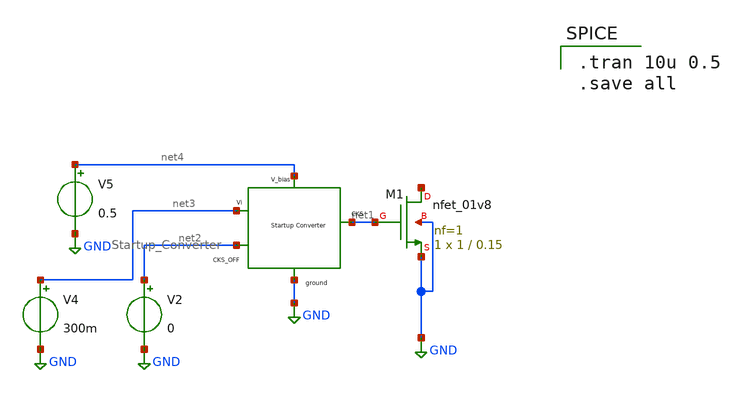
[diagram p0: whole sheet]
** sch_path: Blocks/StartupConverter/Startup_Converter2.sch
**.subckt Startup_Converter2
XM1 net5 net1 GND GND sky130_fd_pr__nfet_01v8 L=0.15 W=1 nf=1 ad='int((nf+1)/2) * W/nf * 0.29' as='int((nf+2)/2) * W/nf * 0.29'
+ pd='2*int((nf+1)/2) * (W/nf + 0.29)' ps='2*int((nf+2)/2) * (W/nf + 0.29)' nrd='0.29 / W' nrs='0.29 / W'
+ sa=0 sb=0 sd=0 mult=1 m=1
V2 net2 GND 0
V4 net3 GND 300m
V5 net4 GND 0.5
x1 net2 net3 net4 GND net1 Startup_Converter
**** begin user architecture code

** opencircuitdesign pdks install
.lib $::SKYWATER_MODELS/sky130.lib.spice tt



.tran 10u 0.5
.save all

**** end user architecture code
**.ends

* expanding   symbol:  Pico_project/StartupConverter/Startup_Converter.sym # of pins=5
** sym_path: Blocks/StartupConverter/Startup_Converter.sym
** sch_path: Blocks/StartupConverter/Startup_Converter.sch
.subckt Startup_Converter CKS_OFF VP V_bias VN CKS
*.opin CKS
*.iopin VP
*.iopin VN
*.iopin V_bias
*.ipin CKS_OFF
x3 net5 net1 net10 VN Redn_INV
x5 net1 net2 net9 VN Redn_INV
x6 net2 net3 net8 VN Redn_INV
x7 net3 net4 net7 VN Redn_INV
x8 net4 net5 net6 VN Redn_INV
XM13 net10 CKS_OFF VP VP sky130_fd_pr__pfet_01v8 L=0.15 W=0.63 nf=1 ad='int((nf+1)/2) * W/nf * 0.29'
+ as='int((nf+2)/2) * W/nf * 0.29' pd='2*int((nf+1)/2) * (W/nf + 0.29)' ps='2*int((nf+2)/2) * (W/nf + 0.29)'
+ nrd='0.29 / W' nrs='0.29 / W' sa=0 sb=0 sd=0 mult=1 m=1
XM14 net9 CKS_OFF VP VP sky130_fd_pr__pfet_01v8 L=0.15 W=0.63 nf=1 ad='int((nf+1)/2) * W/nf * 0.29' as='int((nf+2)/2) * W/nf * 0.29'
+ pd='2*int((nf+1)/2) * (W/nf + 0.29)' ps='2*int((nf+2)/2) * (W/nf + 0.29)' nrd='0.29 / W' nrs='0.29 / W'
+ sa=0 sb=0 sd=0 mult=1 m=1
XM15 net8 CKS_OFF VP VP sky130_fd_pr__pfet_01v8 L=0.15 W=0.63 nf=1 ad='int((nf+1)/2) * W/nf * 0.29' as='int((nf+2)/2) * W/nf * 0.29'
+ pd='2*int((nf+1)/2) * (W/nf + 0.29)' ps='2*int((nf+2)/2) * (W/nf + 0.29)' nrd='0.29 / W' nrs='0.29 / W'
+ sa=0 sb=0 sd=0 mult=1 m=1
XM16 net7 CKS_OFF VP VP sky130_fd_pr__pfet_01v8 L=0.15 W=0.63 nf=1 ad='int((nf+1)/2) * W/nf * 0.29' as='int((nf+2)/2) * W/nf * 0.29'
+ pd='2*int((nf+1)/2) * (W/nf + 0.29)' ps='2*int((nf+2)/2) * (W/nf + 0.29)' nrd='0.29 / W' nrs='0.29 / W'
+ sa=0 sb=0 sd=0 mult=1 m=1
XM17 net6 CKS_OFF VP VP sky130_fd_pr__pfet_01v8 L=0.15 W=0.63 nf=1 ad='int((nf+1)/2) * W/nf * 0.29' as='int((nf+2)/2) * W/nf * 0.29'
+ pd='2*int((nf+1)/2) * (W/nf + 0.29)' ps='2*int((nf+2)/2) * (W/nf + 0.29)' nrd='0.29 / W' nrs='0.29 / W'
+ sa=0 sb=0 sd=0 mult=1 m=1
XM18 net12 net11 net13 net13 sky130_fd_pr__pfet_01v8 L=0.15 W=0.42 nf=1 ad='int((nf+1)/2) * W/nf * 0.29'
+ as='int((nf+2)/2) * W/nf * 0.29' pd='2*int((nf+1)/2) * (W/nf + 0.29)' ps='2*int((nf+2)/2) * (W/nf + 0.29)'
+ nrd='0.29 / W' nrs='0.29 / W' sa=0 sb=0 sd=0 mult=1 m=1
XM19 net12 net11 VN VN sky130_fd_pr__nfet_01v8 L=0.15 W=0.42 nf=1 ad='int((nf+1)/2) * W/nf * 0.29' as='int((nf+2)/2) * W/nf * 0.29'
+ pd='2*int((nf+1)/2) * (W/nf + 0.29)' ps='2*int((nf+2)/2) * (W/nf + 0.29)' nrd='0.29 / W' nrs='0.29 / W'
+ sa=0 sb=0 sd=0 mult=1 m=1
XM21 CKS CKS_OFF VN VN sky130_fd_pr__nfet_01v8 L=0.15 W=0.42 nf=1 ad='int((nf+1)/2) * W/nf * 0.29' as='int((nf+2)/2) * W/nf * 0.29'
+ pd='2*int((nf+1)/2) * (W/nf + 0.29)' ps='2*int((nf+2)/2) * (W/nf + 0.29)' nrd='0.29 / W' nrs='0.29 / W'
+ sa=0 sb=0 sd=0 mult=1 m=1
XM20 CKS CKS_OFF net12 net12 sky130_fd_pr__pfet_01v8 L=0.15 W=0.42 nf=1 ad='int((nf+1)/2) * W/nf * 0.29'
+ as='int((nf+2)/2) * W/nf * 0.29' pd='2*int((nf+1)/2) * (W/nf + 0.29)' ps='2*int((nf+2)/2) * (W/nf + 0.29)'
+ nrd='0.29 / W' nrs='0.29 / W' sa=0 sb=0 sd=0 mult=1 m=1
x1 net5 VP VN net13 net11 V_bias Clk_Booster_Updated
.ends


* expanding   symbol:  Pico_project/Rdn_INV/Redn_INV.sym # of pins=4
** sym_path: component/Reduntant_Inverter/Redn_INV.sym
** sch_path: component/Reduntant_Inverter/Redn_INV.sch
.subckt Redn_INV X Y VP VN
*.opin Y
*.ipin X
*.iopin VP
*.iopin VN
XM15 net4 X VN VN sky130_fd_pr__nfet_01v8_lvt L=0.15 W=1 nf=1 ad='int((nf+1)/2) * W/nf * 0.29' as='int((nf+2)/2) * W/nf * 0.29'
+ pd='2*int((nf+1)/2) * (W/nf + 0.29)' ps='2*int((nf+2)/2) * (W/nf + 0.29)' nrd='0.29 / W' nrs='0.29 / W'
+ sa=0 sb=0 sd=0 mult=1 m=1
XM1 net5 X net3 VN sky130_fd_pr__nfet_01v8_lvt L=0.15 W=3.25 nf=1 ad='int((nf+1)/2) * W/nf * 0.29' as='int((nf+2)/2) * W/nf * 0.29'
+ pd='2*int((nf+1)/2) * (W/nf + 0.29)' ps='2*int((nf+2)/2) * (W/nf + 0.29)' nrd='0.29 / W' nrs='0.29 / W'
+ sa=0 sb=0 sd=0 mult=1 m=1
XM16 Y X net6 VN sky130_fd_pr__nfet_01v8_lvt L=0.15 W=6.5 nf=1 ad='int((nf+1)/2) * W/nf * 0.29' as='int((nf+2)/2) * W/nf * 0.29'
+ pd='2*int((nf+1)/2) * (W/nf + 0.29)' ps='2*int((nf+2)/2) * (W/nf + 0.29)' nrd='0.29 / W' nrs='0.29 / W'
+ sa=0 sb=0 sd=0 mult=1 m=1
XM17 net3 X VN VN sky130_fd_pr__nfet_01v8_lvt L=0.15 W=3.25 nf=1 ad='int((nf+1)/2) * W/nf * 0.29' as='int((nf+2)/2) * W/nf * 0.29'
+ pd='2*int((nf+1)/2) * (W/nf + 0.29)' ps='2*int((nf+2)/2) * (W/nf + 0.29)' nrd='0.29 / W' nrs='0.29 / W'
+ sa=0 sb=0 sd=0 mult=1 m=1
XM18 net2 X VN VN sky130_fd_pr__nfet_01v8_lvt L=0.15 W=1.5 nf=1 ad='int((nf+1)/2) * W/nf * 0.29' as='int((nf+2)/2) * W/nf * 0.29'
+ pd='2*int((nf+1)/2) * (W/nf + 0.29)' ps='2*int((nf+2)/2) * (W/nf + 0.29)' nrd='0.29 / W' nrs='0.29 / W'
+ sa=0 sb=0 sd=0 mult=1 m=1
XM19 net1 X VN VN sky130_fd_pr__nfet_01v8_lvt L=0.15 W=6.5 nf=1 ad='int((nf+1)/2) * W/nf * 0.29' as='int((nf+2)/2) * W/nf * 0.29'
+ pd='2*int((nf+1)/2) * (W/nf + 0.29)' ps='2*int((nf+2)/2) * (W/nf + 0.29)' nrd='0.29 / W' nrs='0.29 / W'
+ sa=0 sb=0 sd=0 mult=1 m=1
XM20 net6 X net1 VN sky130_fd_pr__nfet_01v8_lvt L=0.15 W=6.5 nf=1 ad='int((nf+1)/2) * W/nf * 0.29' as='int((nf+2)/2) * W/nf * 0.29'
+ pd='2*int((nf+1)/2) * (W/nf + 0.29)' ps='2*int((nf+2)/2) * (W/nf + 0.29)' nrd='0.29 / W' nrs='0.29 / W'
+ sa=0 sb=0 sd=0 mult=1 m=1
XM2 net4 X VP VP sky130_fd_pr__pfet_01v8 L=0.15 W=10 nf=1 ad='int((nf+1)/2) * W/nf * 0.29' as='int((nf+2)/2) * W/nf * 0.29'
+ pd='2*int((nf+1)/2) * (W/nf + 0.29)' ps='2*int((nf+2)/2) * (W/nf + 0.29)' nrd='0.29 / W' nrs='0.29 / W'
+ sa=0 sb=0 sd=0 mult=1 m=1
XM5 net5 X net4 net4 sky130_fd_pr__pfet_01v8 L=0.15 W=10 nf=1 ad='int((nf+1)/2) * W/nf * 0.29' as='int((nf+2)/2) * W/nf * 0.29'
+ pd='2*int((nf+1)/2) * (W/nf + 0.29)' ps='2*int((nf+2)/2) * (W/nf + 0.29)' nrd='0.29 / W' nrs='0.29 / W'
+ sa=0 sb=0 sd=0 mult=1 m=1
XM6 Y X net5 VP sky130_fd_pr__pfet_01v8 L=0.15 W=10 nf=1 ad='int((nf+1)/2) * W/nf * 0.29' as='int((nf+2)/2) * W/nf * 0.29'
+ pd='2*int((nf+1)/2) * (W/nf + 0.29)' ps='2*int((nf+2)/2) * (W/nf + 0.29)' nrd='0.29 / W' nrs='0.29 / W'
+ sa=0 sb=0 sd=0 mult=1 m=1
XM8 net3 X VP VP sky130_fd_pr__pfet_01v8 L=0.15 W=2 nf=1 ad='int((nf+1)/2) * W/nf * 0.29' as='int((nf+2)/2) * W/nf * 0.29'
+ pd='2*int((nf+1)/2) * (W/nf + 0.29)' ps='2*int((nf+2)/2) * (W/nf + 0.29)' nrd='0.29 / W' nrs='0.29 / W'
+ sa=0 sb=0 sd=0 mult=1 m=1
XM12 net2 X VP VP sky130_fd_pr__pfet_01v8 L=0.15 W=5 nf=1 ad='int((nf+1)/2) * W/nf * 0.29' as='int((nf+2)/2) * W/nf * 0.29'
+ pd='2*int((nf+1)/2) * (W/nf + 0.29)' ps='2*int((nf+2)/2) * (W/nf + 0.29)' nrd='0.29 / W' nrs='0.29 / W'
+ sa=0 sb=0 sd=0 mult=1 m=1
XM14 net6 X net2 VP sky130_fd_pr__pfet_01v8 L=0.15 W=5 nf=1 ad='int((nf+1)/2) * W/nf * 0.29' as='int((nf+2)/2) * W/nf * 0.29'
+ pd='2*int((nf+1)/2) * (W/nf + 0.29)' ps='2*int((nf+2)/2) * (W/nf + 0.29)' nrd='0.29 / W' nrs='0.29 / W'
+ sa=0 sb=0 sd=0 mult=1 m=1
XM21 net1 X VP VP sky130_fd_pr__pfet_01v8 L=0.15 W=1.5 nf=1 ad='int((nf+1)/2) * W/nf * 0.29' as='int((nf+2)/2) * W/nf * 0.29'
+ pd='2*int((nf+1)/2) * (W/nf + 0.29)' ps='2*int((nf+2)/2) * (W/nf + 0.29)' nrd='0.29 / W' nrs='0.29 / W'
+ sa=0 sb=0 sd=0 mult=1 m=1
.ends


* expanding   symbol:  Pico_project/Clock_Booster_new/Clk_Booster_Updated.sym # of pins=6
** sym_path: Blocks/Clock_Booster_new/Clk_Booster_Updated.sym
** sch_path: Blocks/Clock_Booster_new/Clk_Booster_Updated.sch
.subckt Clk_Booster_Updated X VP VN CKP CKN V_bias
*.opin CKP
*.opin CKN
*.iopin VP
*.iopin V_bias
*.ipin X
*.iopin VN
C1 net23 net13 100f m=1
XM1 net15 net6 net11 V_bias sky130_fd_pr__pfet_01v8 L=0.15 W=0.42 nf=1 ad='int((nf+1)/2) * W/nf * 0.29'
+ as='int((nf+2)/2) * W/nf * 0.29' pd='2*int((nf+1)/2) * (W/nf + 0.29)' ps='2*int((nf+2)/2) * (W/nf + 0.29)'
+ nrd='0.29 / W' nrs='0.29 / W' sa=0 sb=0 sd=0 mult=1 m=1
XM3 net6 net5 net24 V_bias sky130_fd_pr__pfet_01v8 L=0.15 W=0.42 nf=1 ad='int((nf+1)/2) * W/nf * 0.29'
+ as='int((nf+2)/2) * W/nf * 0.29' pd='2*int((nf+1)/2) * (W/nf + 0.29)' ps='2*int((nf+2)/2) * (W/nf + 0.29)'
+ nrd='0.29 / W' nrs='0.29 / W' sa=0 sb=0 sd=0 mult=1 m=1
XM4 net6 net5 VN VN sky130_fd_pr__nfet_01v8 L=0.15 W=2 nf=1 ad='int((nf+1)/2) * W/nf * 0.29' as='int((nf+2)/2) * W/nf * 0.29'
+ pd='2*int((nf+1)/2) * (W/nf + 0.29)' ps='2*int((nf+2)/2) * (W/nf + 0.29)' nrd='0.29 / W' nrs='0.29 / W'
+ sa=0 sb=0 sd=0 mult=1 m=1
XM2 net16 CKP net14 V_bias sky130_fd_pr__pfet_01v8 L=0.15 W=0.42 nf=1 ad='int((nf+1)/2) * W/nf * 0.29'
+ as='int((nf+2)/2) * W/nf * 0.29' pd='2*int((nf+1)/2) * (W/nf + 0.29)' ps='2*int((nf+2)/2) * (W/nf + 0.29)'
+ nrd='0.29 / W' nrs='0.29 / W' sa=0 sb=0 sd=0 mult=1 m=1
XM5 CKP net5 net25 V_bias sky130_fd_pr__pfet_01v8 L=0.15 W=0.42 nf=1 ad='int((nf+1)/2) * W/nf * 0.29'
+ as='int((nf+2)/2) * W/nf * 0.29' pd='2*int((nf+1)/2) * (W/nf + 0.29)' ps='2*int((nf+2)/2) * (W/nf + 0.29)'
+ nrd='0.29 / W' nrs='0.29 / W' sa=0 sb=0 sd=0 mult=1 m=1
XM6 CKP net5 VN VN sky130_fd_pr__nfet_01v8 L=0.15 W=1.26 nf=1 ad='int((nf+1)/2) * W/nf * 0.29' as='int((nf+2)/2) * W/nf * 0.29'
+ pd='2*int((nf+1)/2) * (W/nf + 0.29)' ps='2*int((nf+2)/2) * (W/nf + 0.29)' nrd='0.29 / W' nrs='0.29 / W'
+ sa=0 sb=0 sd=0 mult=1 m=1
C3 net10 net7 100f m=1
XM8 net22 net4 net7 V_bias sky130_fd_pr__pfet_01v8 L=0.15 W=0.42 nf=1 ad='int((nf+1)/2) * W/nf * 0.29'
+ as='int((nf+2)/2) * W/nf * 0.29' pd='2*int((nf+1)/2) * (W/nf + 0.29)' ps='2*int((nf+2)/2) * (W/nf + 0.29)'
+ nrd='0.29 / W' nrs='0.29 / W' sa=0 sb=0 sd=0 mult=1 m=1
XM9 net9 net4 VN VN sky130_fd_pr__nfet_01v8 L=0.15 W=2 nf=1 ad='int((nf+1)/2) * W/nf * 0.29' as='int((nf+2)/2) * W/nf * 0.29'
+ pd='2*int((nf+1)/2) * (W/nf + 0.29)' ps='2*int((nf+2)/2) * (W/nf + 0.29)' nrd='0.29 / W' nrs='0.29 / W'
+ sa=0 sb=0 sd=0 mult=1 m=1
XM10 net8 CKN net18 V_bias sky130_fd_pr__pfet_01v8 L=0.15 W=0.42 nf=1 ad='int((nf+1)/2) * W/nf * 0.29'
+ as='int((nf+2)/2) * W/nf * 0.29' pd='2*int((nf+1)/2) * (W/nf + 0.29)' ps='2*int((nf+2)/2) * (W/nf + 0.29)'
+ nrd='0.29 / W' nrs='0.29 / W' sa=0 sb=0 sd=0 mult=1 m=1
XM11 net21 net4 net8 V_bias sky130_fd_pr__pfet_01v8 L=0.15 W=0.42 nf=1 ad='int((nf+1)/2) * W/nf * 0.29'
+ as='int((nf+2)/2) * W/nf * 0.29' pd='2*int((nf+1)/2) * (W/nf + 0.29)' ps='2*int((nf+2)/2) * (W/nf + 0.29)'
+ nrd='0.29 / W' nrs='0.29 / W' sa=0 sb=0 sd=0 mult=1 m=1
XM12 CKN net4 VN VN sky130_fd_pr__nfet_01v8 L=0.15 W=1.26 nf=1 ad='int((nf+1)/2) * W/nf * 0.29' as='int((nf+2)/2) * W/nf * 0.29'
+ pd='2*int((nf+1)/2) * (W/nf + 0.29)' ps='2*int((nf+2)/2) * (W/nf + 0.29)' nrd='0.29 / W' nrs='0.29 / W'
+ sa=0 sb=0 sd=0 mult=1 m=1
C4 net9 net8 100f m=1
XM7 net7 net9 net19 V_bias sky130_fd_pr__pfet_01v8 L=0.15 W=0.42 nf=1 ad='int((nf+1)/2) * W/nf * 0.29'
+ as='int((nf+2)/2) * W/nf * 0.29' pd='2*int((nf+1)/2) * (W/nf + 0.29)' ps='2*int((nf+2)/2) * (W/nf + 0.29)'
+ nrd='0.29 / W' nrs='0.29 / W' sa=0 sb=0 sd=0 mult=1 m=1
x4 net5 net23 VP VN Redn_INV
x1 X net1 VP VN Redn_INV
x2 net1 net2 VP VN Redn_INV
x15 net2 net5 VP VN Redn_INV
x22 net3 net4 VP VN Redn_INV
x23 net4 net10 VP VN Redn_INV
XM18 net13 net6 net15 V_bias sky130_fd_pr__pfet_01v8 L=0.15 W=0.42 nf=1 ad='int((nf+1)/2) * W/nf * 0.29'
+ as='int((nf+2)/2) * W/nf * 0.29' pd='2*int((nf+1)/2) * (W/nf + 0.29)' ps='2*int((nf+2)/2) * (W/nf + 0.29)'
+ nrd='0.29 / W' nrs='0.29 / W' sa=0 sb=0 sd=0 mult=1 m=1
XM21 net12 CKP net16 V_bias sky130_fd_pr__pfet_01v8 L=0.15 W=0.42 nf=1 ad='int((nf+1)/2) * W/nf * 0.29'
+ as='int((nf+2)/2) * W/nf * 0.29' pd='2*int((nf+1)/2) * (W/nf + 0.29)' ps='2*int((nf+2)/2) * (W/nf + 0.29)'
+ nrd='0.29 / W' nrs='0.29 / W' sa=0 sb=0 sd=0 mult=1 m=1
C2 net6 net12 100f m=1
XM19 net11 net6 VP V_bias sky130_fd_pr__pfet_01v8 L=0.15 W=0.42 nf=1 ad='int((nf+1)/2) * W/nf * 0.29'
+ as='int((nf+2)/2) * W/nf * 0.29' pd='2*int((nf+1)/2) * (W/nf + 0.29)' ps='2*int((nf+2)/2) * (W/nf + 0.29)'
+ nrd='0.29 / W' nrs='0.29 / W' sa=0 sb=0 sd=0 mult=1 m=1
XM20 net14 CKP VP V_bias sky130_fd_pr__pfet_01v8 L=0.15 W=0.42 nf=1 ad='int((nf+1)/2) * W/nf * 0.29'
+ as='int((nf+2)/2) * W/nf * 0.29' pd='2*int((nf+1)/2) * (W/nf + 0.29)' ps='2*int((nf+2)/2) * (W/nf + 0.29)'
+ nrd='0.29 / W' nrs='0.29 / W' sa=0 sb=0 sd=0 mult=1 m=1
XM22 net25 net5 net12 V_bias sky130_fd_pr__pfet_01v8 L=0.15 W=0.42 nf=1 ad='int((nf+1)/2) * W/nf * 0.29'
+ as='int((nf+2)/2) * W/nf * 0.29' pd='2*int((nf+1)/2) * (W/nf + 0.29)' ps='2*int((nf+2)/2) * (W/nf + 0.29)'
+ nrd='0.29 / W' nrs='0.29 / W' sa=0 sb=0 sd=0 mult=1 m=1
XM23 net24 net5 net13 V_bias sky130_fd_pr__pfet_01v8 L=0.15 W=0.42 nf=1 ad='int((nf+1)/2) * W/nf * 0.29'
+ as='int((nf+2)/2) * W/nf * 0.29' pd='2*int((nf+1)/2) * (W/nf + 0.29)' ps='2*int((nf+2)/2) * (W/nf + 0.29)'
+ nrd='0.29 / W' nrs='0.29 / W' sa=0 sb=0 sd=0 mult=1 m=1
XM24 net19 net9 net20 V_bias sky130_fd_pr__pfet_01v8 L=0.15 W=0.42 nf=1 ad='int((nf+1)/2) * W/nf * 0.29'
+ as='int((nf+2)/2) * W/nf * 0.29' pd='2*int((nf+1)/2) * (W/nf + 0.29)' ps='2*int((nf+2)/2) * (W/nf + 0.29)'
+ nrd='0.29 / W' nrs='0.29 / W' sa=0 sb=0 sd=0 mult=1 m=1
XM25 net20 net9 VP V_bias sky130_fd_pr__pfet_01v8 L=0.15 W=0.42 nf=1 ad='int((nf+1)/2) * W/nf * 0.29'
+ as='int((nf+2)/2) * W/nf * 0.29' pd='2*int((nf+1)/2) * (W/nf + 0.29)' ps='2*int((nf+2)/2) * (W/nf + 0.29)'
+ nrd='0.29 / W' nrs='0.29 / W' sa=0 sb=0 sd=0 mult=1 m=1
XM26 net18 CKN net17 V_bias sky130_fd_pr__pfet_01v8 L=0.15 W=0.42 nf=1 ad='int((nf+1)/2) * W/nf * 0.29'
+ as='int((nf+2)/2) * W/nf * 0.29' pd='2*int((nf+1)/2) * (W/nf + 0.29)' ps='2*int((nf+2)/2) * (W/nf + 0.29)'
+ nrd='0.29 / W' nrs='0.29 / W' sa=0 sb=0 sd=0 mult=1 m=1
XM27 net17 CKN VP V_bias sky130_fd_pr__pfet_01v8 L=0.15 W=0.42 nf=1 ad='int((nf+1)/2) * W/nf * 0.29'
+ as='int((nf+2)/2) * W/nf * 0.29' pd='2*int((nf+1)/2) * (W/nf + 0.29)' ps='2*int((nf+2)/2) * (W/nf + 0.29)'
+ nrd='0.29 / W' nrs='0.29 / W' sa=0 sb=0 sd=0 mult=1 m=1
XM28 net9 net4 net22 V_bias sky130_fd_pr__pfet_01v8 L=0.15 W=0.42 nf=1 ad='int((nf+1)/2) * W/nf * 0.29'
+ as='int((nf+2)/2) * W/nf * 0.29' pd='2*int((nf+1)/2) * (W/nf + 0.29)' ps='2*int((nf+2)/2) * (W/nf + 0.29)'
+ nrd='0.29 / W' nrs='0.29 / W' sa=0 sb=0 sd=0 mult=1 m=1
XM29 CKN net4 net21 V_bias sky130_fd_pr__pfet_01v8 L=0.15 W=0.42 nf=1 ad='int((nf+1)/2) * W/nf * 0.29'
+ as='int((nf+2)/2) * W/nf * 0.29' pd='2*int((nf+1)/2) * (W/nf + 0.29)' ps='2*int((nf+2)/2) * (W/nf + 0.29)'
+ nrd='0.29 / W' nrs='0.29 / W' sa=0 sb=0 sd=0 mult=1 m=1
x9 net2 net3 VP VN Redn_INV
.ends

.GLOBAL GND
.end
